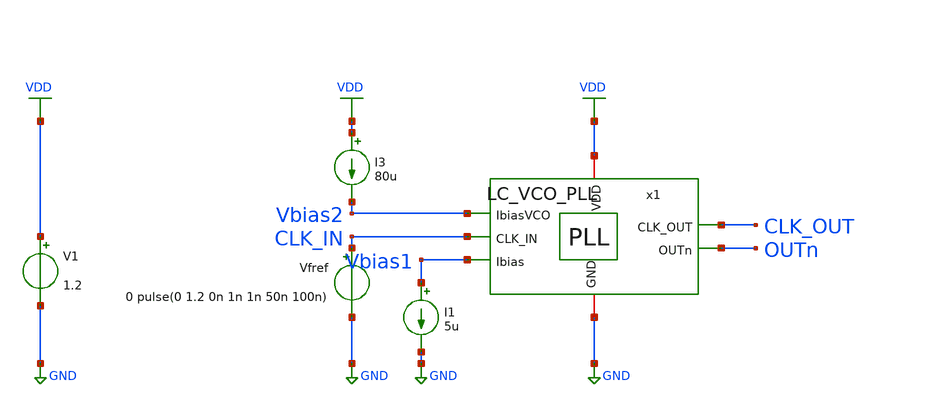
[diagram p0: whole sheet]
** sch_path: schematic/top-pll/LC_VCO_PLL_tb.sch
**.subckt LC_VCO_PLL_tb
V1 VDD GND 1.2
Vfref CLK_IN GND 0 pulse(0 1.2 0n 1n 1n 50n 100n)
I1 Vbias1 GND 5u
x1 VDD CLK_IN CLK_OUT Vbias2 OUTn Vbias1 GND LC_VCO_PLL
I3 VDD Vbias2 80u
**** begin user architecture code



*****************************************************
* PLL + DSM Frequency Divider Testbench (Optimized)
*****************************************************

.option temp=27
.param VDD=1.2

* ==============================
* Include Models & Stimuli
* ==============================
.include ./IHP_4nH_Inductor.spice
.include stimuli_test.cir

* ==============================
* Simulation Options (Optimized for Speed & Stability)
* ==============================
* gear method improves stability for long oscillator runs
* reltol=1e-3 prevents the simulator from bogging down on microscopic errors
.options reltol=1e-3 abstol=1e-9 vntol=1e-6 method=gear

* ==============================
* Initial Conditions (Speed Hack)
* ==============================
* Uncomment the line below to pre-charge the loop filter to your expected
* V_tune voltage (e.g., 0.6V). This skips the massive initial frequency jump.
.ic v(x2.vctrl)=0.606
.ic v(x2.x1.ctrl1)=0.606
.ic v(x2.x1.ctrl2)=0.606
.op
*.nodeset v(x2.vctrl)=0.606
*.nodeset v(x2.x1.ctrl1)=0.606
*.nodeset v(x2.x1.ctrl2)=0.606

.control
  * CRITICAL: Save ONLY essential low-frequency signals.
  * Saving 2.4GHz nodes for 100us will crash your memory.
  save x2.vctrl x2.up x2.dn x2.dsm_out clk_out clk_in vbias1 vbias2 x2.x1.ctrl1 x2.x1.ctrl2
  *save all


  * 20p defines the step to resolve the 2.4 GHz edges without forcing a maxstep.
  tran 30p 30u uic

  remzerovec
  write pll_top.raw
.endc






.lib cornerMOSlv.lib mos_tt
.lib cornerMOShv.lib mos_tt
.lib cornerHBT.lib hbt_typ
.lib cornerRES.lib res_typ
.lib cornerCAP.lib cap_typ_stat
.include /foss/pdks/ihp-sg13g2/libs.ref/sg13g2_stdcell/spice/sg13g2_stdcell.spice
.global VDD GND


.param CP_N_L = 1u
.param CP_N_W = 3u
.param CP_P_M = 1
.param CP_P_L = 1u
.param CP_P_W = 10u
.param CP_N_M = 1



**** end user architecture code
**.ends
.GLOBAL GND
.GLOBAL VDD
.end
